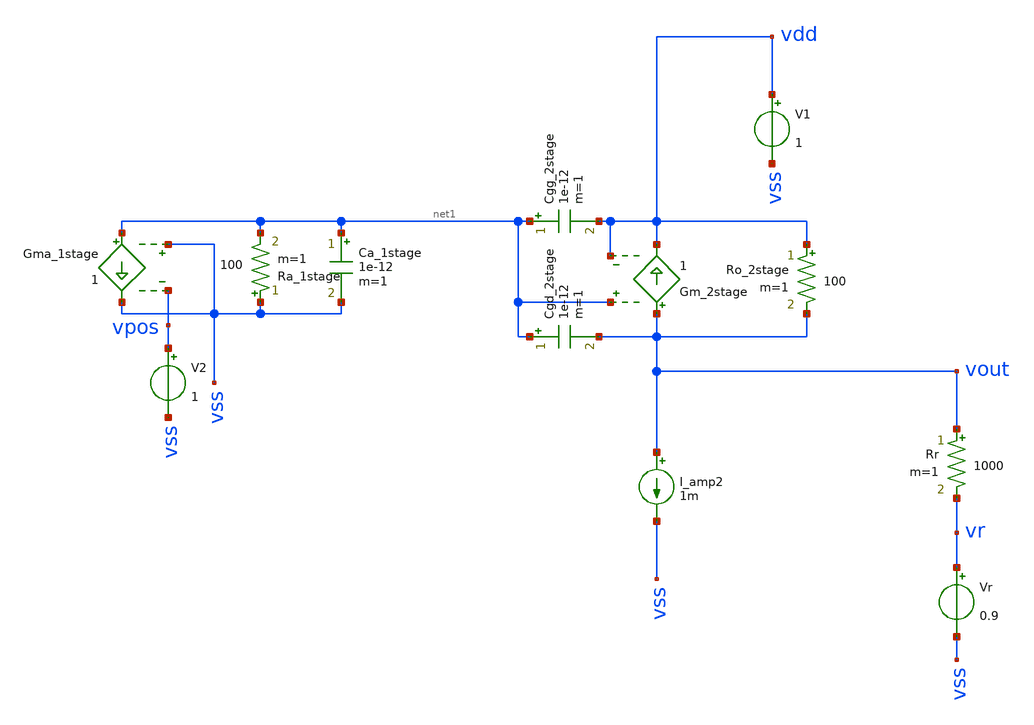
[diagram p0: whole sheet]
** sch_path: test/Tesis_notebooks/xschem/ota_2stage_rout.sch
**.subckt ota_2stage_rout
Ro_2stage vdd vout 100 m=1
Gm_2stage vout vdd net1 vdd 1
Gma_1stage net1 vss vss vpos 1
Ra_1stage vss net1 100 m=1
V1 vdd vss 1
Cgg_2stage net1 vdd 1e-12 m=1
Cgd_2stage net1 vout 1e-12 m=1
Ca_1stage net1 vss 1e-12 m=1
V2 vpos vss 1
I_amp2 vout vss 1m
Vr vr vss 0.9
Rr vout vr 1000 m=1
**.ends
.end
